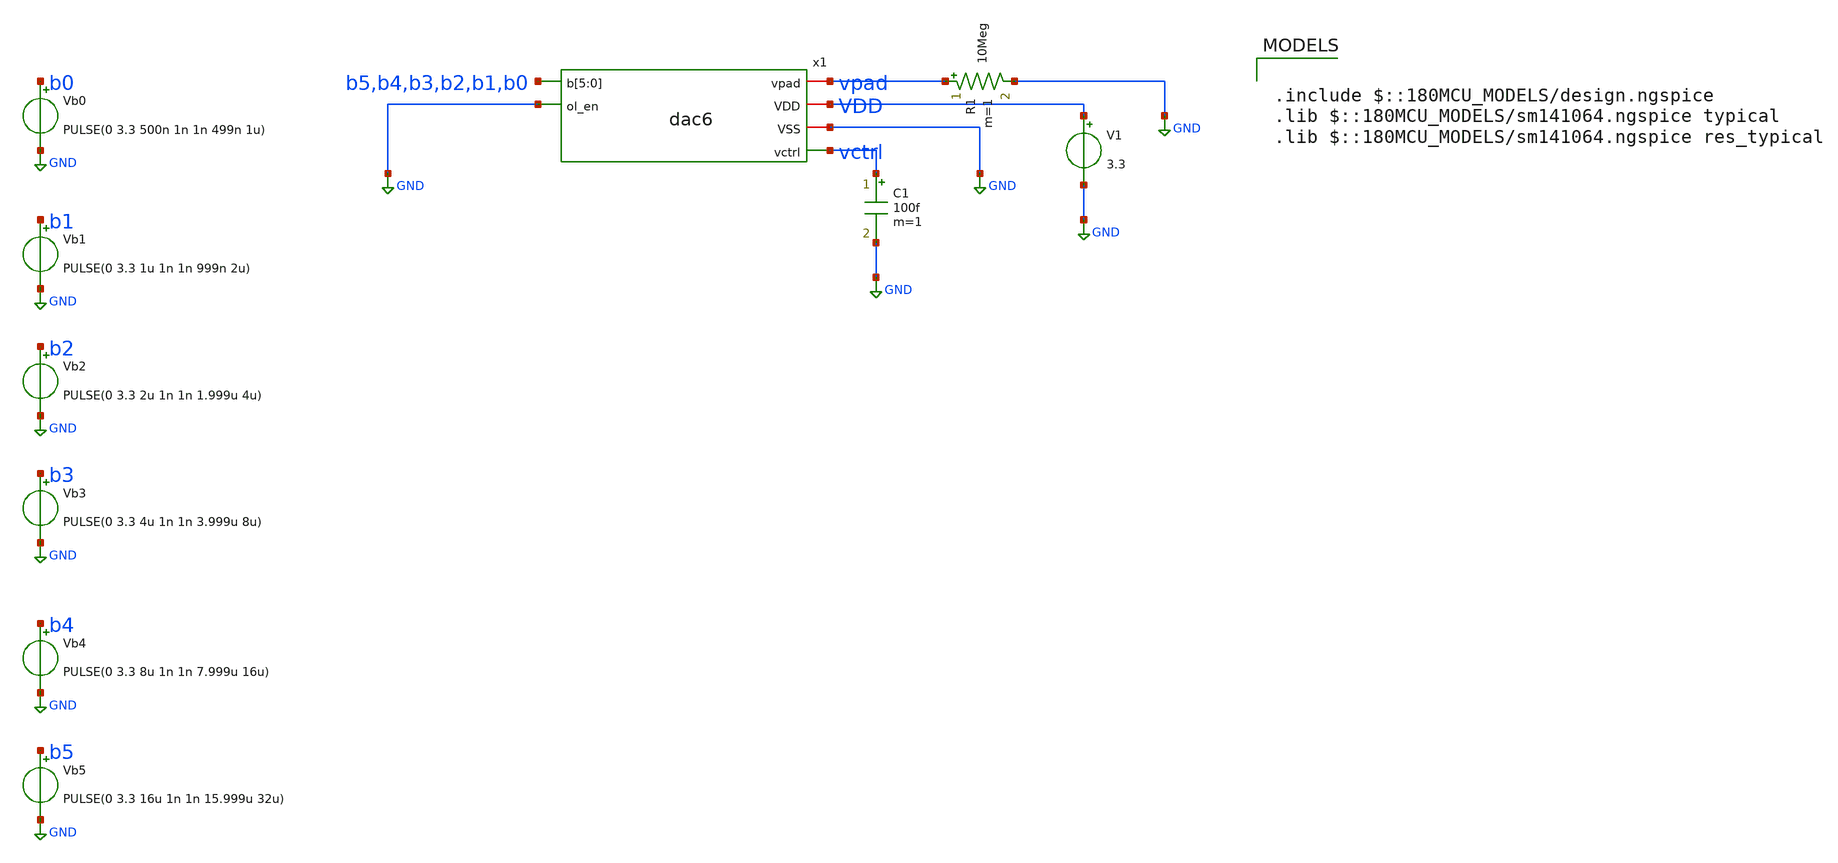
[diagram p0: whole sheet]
** sch_path: xschem/pll_dac/tb_dac6_static.sch
**.subckt tb_dac6_static
x1 b5 b4 b3 b2 b1 b0 GND vpad VDD GND vctrl dac6
V1 VDD GND 3.3
C1 vctrl GND 100f m=1
R1 vpad GND 10Meg m=1
Vb0 b0 GND PULSE(0 3.3 500n 1n 1n 499n 1u)
Vb2 b2 GND PULSE(0 3.3 2u 1n 1n 1.999u 4u)
Vb1 b1 GND PULSE(0 3.3 1u 1n 1n 999n 2u)
Vb3 b3 GND PULSE(0 3.3 4u 1n 1n 3.999u 8u)
Vb4 b4 GND PULSE(0 3.3 8u 1n 1n 7.999u 16u)
Vb5 b5 GND PULSE(0 3.3 16u 1n 1n 15.999u 32u)
**** begin user architecture code

.include $::180MCU_MODELS/design.ngspice
.lib $::180MCU_MODELS/sm141064.ngspice typical
.lib $::180MCU_MODELS/sm141064.ngspice res_typical



.control
save v(vctrl) i(V1)
tran 1n 32u
plot v(vctrl) title 'VCTRL vs time'
linearize v(vctrl) i(V1)
let vcode = vector(64)
let icode = vector(64)
let k = 0
while k < 64
  let idx = (k+1)*500 - 25
  let vcode[k] = v(vctrl)[idx]
  let icode[k] = -i(V1)[idx]
  let k = k + 1
end
let lsb = (vcode[63] - vcode[0]) / 63
let code = vector(64)
let trans = vector(63)
let stp = vcode[1,63] - vcode[0,62]
let dnl = stp / lsb - 1
let inl = (vcode - (vcode[0] + lsb * code)) / lsb
let worst = vecmin(dnl)
let k = 0
while k < 63
  if dnl[k] = worst
    let wcode = k
  end
  let k = k + 1
end
let wnext = wcode + 1
let v0 = vcode[0]
let v63 = vcode[63]
let lsbmv = abs(lsb) * 1000
let dmax = vecmax(dnl)
let imin = vecmin(inl)
let imx = vecmax(inl)
let d7 = dnl[7]
let d15 = dnl[15]
let d31 = dnl[31]
let d47 = dnl[47]
let iua = vecmax(icode) * 1e6
echo =================== DAC static results ===================
echo V(code 0) = $&v0 V     V(code 63) = $&v63 V
echo LSB        = $&lsbmv mV
echo Worst DNL  = $&worst LSB  (at code $&wcode to $&wnext)
echo Max DNL    = $&dmax LSB
echo INL range  = $&imin to $&imx LSB
echo Major carries:  7-8: $&d7   15-16: $&d15   31-32: $&d31   47-48: $&d47
echo Highest settled supply current = $&iua uA
if worst > -1
  echo MONOTONIC: yes (every step goes the same way)
else
  echo MONOTONIC: NO, at least one step goes backwards
end
echo ==========================================================
plot vcode vs code title 'VCTRL at each code' xlabel 'code' ylabel 'V'
plot dnl vs trans title 'DNL per step (step k to k+1)' xlabel 'step k' ylabel 'LSB'
plot inl vs code title 'INL per code' xlabel 'code' ylabel 'LSB'
.endc


**** end user architecture code
**.ends

* expanding   symbol:  pll_dac/dac6.sym # of pins=6
** sym_path: xschem/pll_dac/dac6.sym
** sch_path: xschem/pll_dac/dac6.sch
.subckt dac6 b[5] b[4] b[3] b[2] b[1] b[0] ol_en vpad VDD VSS vctrl
*.ipin b[5],b[4],b[3],b[2],b[1],b[0]
*.ipin ol_en
*.iopin vpad
*.iopin VDD
*.iopin VSS
*.opin vctrl
x1 VDD b[5] b[4] b[3] b[2] b[1] b[0] VSS vctrl schr2r6
XRD1 rd vctrl VSS ppolyf_u_1k r_width=1u r_length=61u m=1
XRD2[1] VSS rd VSS ppolyf_u_1k r_width=1u r_length=61u m=1
XRD2[0] VSS rd VSS ppolyf_u_1k r_width=1u r_length=61u m=1
XOL VDD ol_en ol_en_b VSS sw_inv
XM2 vctrl ol_en_b vpad VDD pfet_03v3 L=0.28u W=5.6u nf=1 ad='int((nf+1)/2) * W/nf * 0.18u' as='int((nf+2)/2) * W/nf * 0.18u'
+ pd='2*int((nf+1)/2) * (W/nf + 0.18u)' ps='2*int((nf+2)/2) * (W/nf + 0.18u)' nrd='0.18u / W' nrs='0.18u / W'
+ sa=0 sb=0 sd=0 m=1
XM1 vctrl ol_en vpad VSS nfet_03v3 L=0.28u W=2u nf=1 ad='int((nf+1)/2) * W/nf * 0.18u' as='int((nf+2)/2) * W/nf * 0.18u'
+ pd='2*int((nf+1)/2) * (W/nf + 0.18u)' ps='2*int((nf+2)/2) * (W/nf + 0.18u)' nrd='0.18u / W' nrs='0.18u / W'
+ sa=0 sb=0 sd=0 m=1
.ends


* expanding   symbol:  pll_dac/schr2r6.sym # of pins=4
** sym_path: xschem/pll_dac/schr2r6.sym
** sch_path: xschem/pll_dac/schr2r6.sch
.subckt schr2r6 VDD b[5] b[4] b[3] b[2] b[1] b[0] VSS lad
*.iopin VDD
*.iopin VSS
*.ipin b[5],b[4],b[3],b[2],b[1],b[0]
*.opin lad
XI[5] VDD b[5] d[5] VSS sw_inv
XI[4] VDD b[4] d[4] VSS sw_inv
XI[3] VDD b[3] d[3] VSS sw_inv
XI[2] VDD b[2] d[2] VSS sw_inv
XI[1] VDD b[1] d[1] VSS sw_inv
XI[0] VDD b[0] d[0] VSS sw_inv
XIT VDD VDD dt VSS sw_inv
XRLa[5] m[5] d[5] VSS ppolyf_u_1k r_width=1u r_length=61u m=1
XRLa[4] m[4] d[4] VSS ppolyf_u_1k r_width=1u r_length=61u m=1
XRLa[3] m[3] d[3] VSS ppolyf_u_1k r_width=1u r_length=61u m=1
XRLa[2] m[2] d[2] VSS ppolyf_u_1k r_width=1u r_length=61u m=1
XRLa[1] m[1] d[1] VSS ppolyf_u_1k r_width=1u r_length=61u m=1
XRLa[0] m[0] d[0] VSS ppolyf_u_1k r_width=1u r_length=61u m=1
XRLb[5] lad m[5] VSS ppolyf_u_1k r_width=1u r_length=61u m=1
XRLb[4] j[4] m[4] VSS ppolyf_u_1k r_width=1u r_length=61u m=1
XRLb[3] j[3] m[3] VSS ppolyf_u_1k r_width=1u r_length=61u m=1
XRLb[2] j[2] m[2] VSS ppolyf_u_1k r_width=1u r_length=61u m=1
XRLb[1] j[1] m[1] VSS ppolyf_u_1k r_width=1u r_length=61u m=1
XRLb[0] j[0] m[0] VSS ppolyf_u_1k r_width=1u r_length=61u m=1
XRR[4] lad j[4] VSS ppolyf_u_1k r_width=1u r_length=61u m=1
XRR[3] j[4] j[3] VSS ppolyf_u_1k r_width=1u r_length=61u m=1
XRR[2] j[3] j[2] VSS ppolyf_u_1k r_width=1u r_length=61u m=1
XRR[1] j[2] j[1] VSS ppolyf_u_1k r_width=1u r_length=61u m=1
XRR[0] j[1] j[0] VSS ppolyf_u_1k r_width=1u r_length=61u m=1
XRTa mt dt VSS ppolyf_u_1k r_width=1u r_length=61u m=1
XRTb j[0] mt VSS ppolyf_u_1k r_width=1u r_length=61u m=1
XRDUM[3] VSS VSS VSS ppolyf_u_1k r_width=1u r_length=61u m=1
XRDUM[2] VSS VSS VSS ppolyf_u_1k r_width=1u r_length=61u m=1
XRDUM[1] VSS VSS VSS ppolyf_u_1k r_width=1u r_length=61u m=1
XRDUM[0] VSS VSS VSS ppolyf_u_1k r_width=1u r_length=61u m=1
.ends


* expanding   symbol:  pll_dac/sw_inv.sym # of pins=4
** sym_path: xschem/pll_dac/sw_inv.sym
** sch_path: xschem/pll_dac/sw_inv.sch
.subckt sw_inv VDD A Y VSS
*.ipin A
*.iopin VDD
*.iopin VSS
*.opin Y
XM1 Y A VSS VSS nfet_03v3 L=0.28u W=2u nf=1 ad='int((nf+1)/2) * W/nf * 0.18u' as='int((nf+2)/2) * W/nf * 0.18u'
+ pd='2*int((nf+1)/2) * (W/nf + 0.18u)' ps='2*int((nf+2)/2) * (W/nf + 0.18u)' nrd='0.18u / W' nrs='0.18u / W'
+ sa=0 sb=0 sd=0 m=1
XM2 Y A VDD VDD pfet_03v3 L=0.28u W=5.6u nf=1 ad='int((nf+1)/2) * W/nf * 0.18u' as='int((nf+2)/2) * W/nf * 0.18u'
+ pd='2*int((nf+1)/2) * (W/nf + 0.18u)' ps='2*int((nf+2)/2) * (W/nf + 0.18u)' nrd='0.18u / W' nrs='0.18u / W'
+ sa=0 sb=0 sd=0 m=1
.ends

.GLOBAL GND
.end
